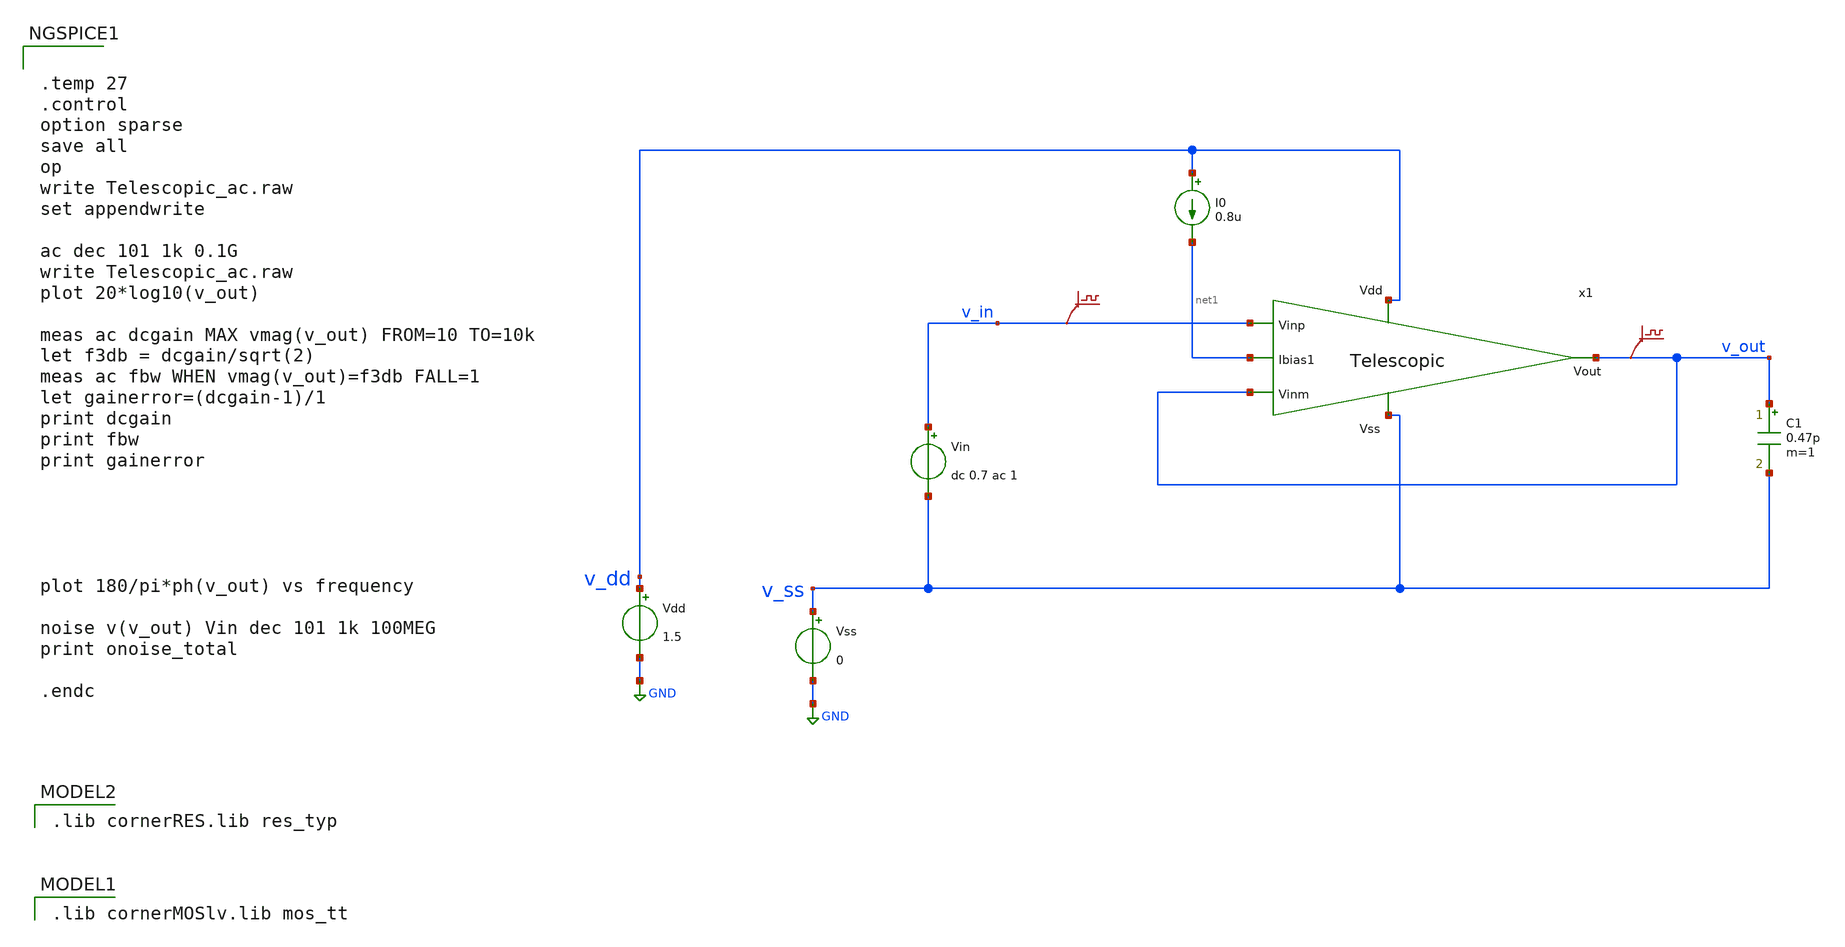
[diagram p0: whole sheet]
** sch_path: DSM/Schematics/Designs_Hrishi/RealCircuits/Telescopic/tb_Telescopic_ac.sch
* (c) 2024 Hrishikesh, @HSB
**.subckt tb_Telescopic_ac
Vss v_ss GND 0
Vdd v_dd GND 1.5
Vin v_in v_ss dc 0.7 ac 1
.save v(v_in)
I0 v_dd net1 0.8u
C1 v_out v_ss 0.47p m=1
.save v(v_out)
x1 v_dd net1 v_out v_out v_in v_ss Telescopic
**** begin user architecture code
 .lib cornerMOSlv.lib mos_tt

 .lib cornerRES.lib res_typ



.temp 27
.control
option sparse
save all
op
write Telescopic_ac.raw
set appendwrite

ac dec 101 1k 0.1G
write Telescopic_ac.raw
plot 20*log10(v_out)

meas ac dcgain MAX vmag(v_out) FROM=10 TO=10k
let f3db = dcgain/sqrt(2)
meas ac fbw WHEN vmag(v_out)=f3db FALL=1
let gainerror=(dcgain-1)/1
print dcgain
print fbw
print gainerror





plot 180/pi*ph(v_out) vs frequency

noise v(v_out) Vin dec 101 1k 100MEG
print onoise_total

.endc


**** end user architecture code
**.ends

* expanding   symbol:
*+  /foss/designs/CEMS_DSM/DSM/Schematics/Designs_Hrishi/RealCircuits/Telescopic/Telescopic.sym # of pins=6
** sym_path: DSM/IC_Designs_Hrishi/RealCircuits/Telescopic/Telescopic.sym
** sch_path: DSM/IC_Designs_Hrishi/RealCircuits/Telescopic/Telescopic.sch
.subckt Telescopic Vdd Ibias1 Vout Vinm Vinp Vss
*.ipin Vinp
*.opin Vout
*.ipin Vinm
*.ipin Vss
*.ipin Vdd
*.ipin Ibias1
XM19 net1 net8 Vss Vss sg13_lv_nmos w=0.272u l=0.2u ng=1 m=1 mm_ok=1
XM11 net2 Vinp net1 Vss sg13_lv_nmos w=0.13u l=0.6u ng=1 m=1 mm_ok=1
XM26 Ibias1 Ibias1 net8 Vss sg13_lv_nmos w=0.13u l=0.6u ng=1 m=1 mm_ok=1
XM27 net8 net8 Vss Vss sg13_lv_nmos w=0.13u l=0.6u ng=1 m=1 mm_ok=1
XM28 net6 net8 Vss Vss sg13_lv_nmos w=0.13u l=0.6u ng=1 m=1 mm_ok=1
XM23 Vout Ibias1 net3 Vss sg13_lv_nmos w=0.13u l=0.6u ng=1 m=1 mm_ok=1
XM14 net3 Vinm net1 Vss sg13_lv_nmos w=0.13u l=0.6u ng=1 m=1 mm_ok=1
XM22 net7 Ibias1 net2 Vss sg13_lv_nmos w=0.13u l=0.6u ng=1 m=1 mm_ok=1
XM29 net7 net7 Vdd Vdd sg13_lv_pmos w=0.375u l=0.4u ng=1 m=1 mm_ok=1
XM30 net6 net6 net7 Vdd sg13_lv_pmos w=0.375u l=0.4u ng=1 m=1 mm_ok=1
XM20 Vout net6 net5 Vdd sg13_lv_pmos w=0.375u l=0.4u ng=1 m=1 mm_ok=1
XM24 net5 net7 Vdd Vdd sg13_lv_pmos w=0.375u l=0.4u ng=1 m=1 mm_ok=1
XM21 net4 net7 Vdd Vdd sg13_lv_pmos w=0.375u l=0.4u ng=1 m=1 mm_ok=1
XM25 net7 net6 net4 Vdd sg13_lv_pmos w=0.375u l=0.4u ng=1 m=1 mm_ok=1
.ends

.GLOBAL GND
.end
